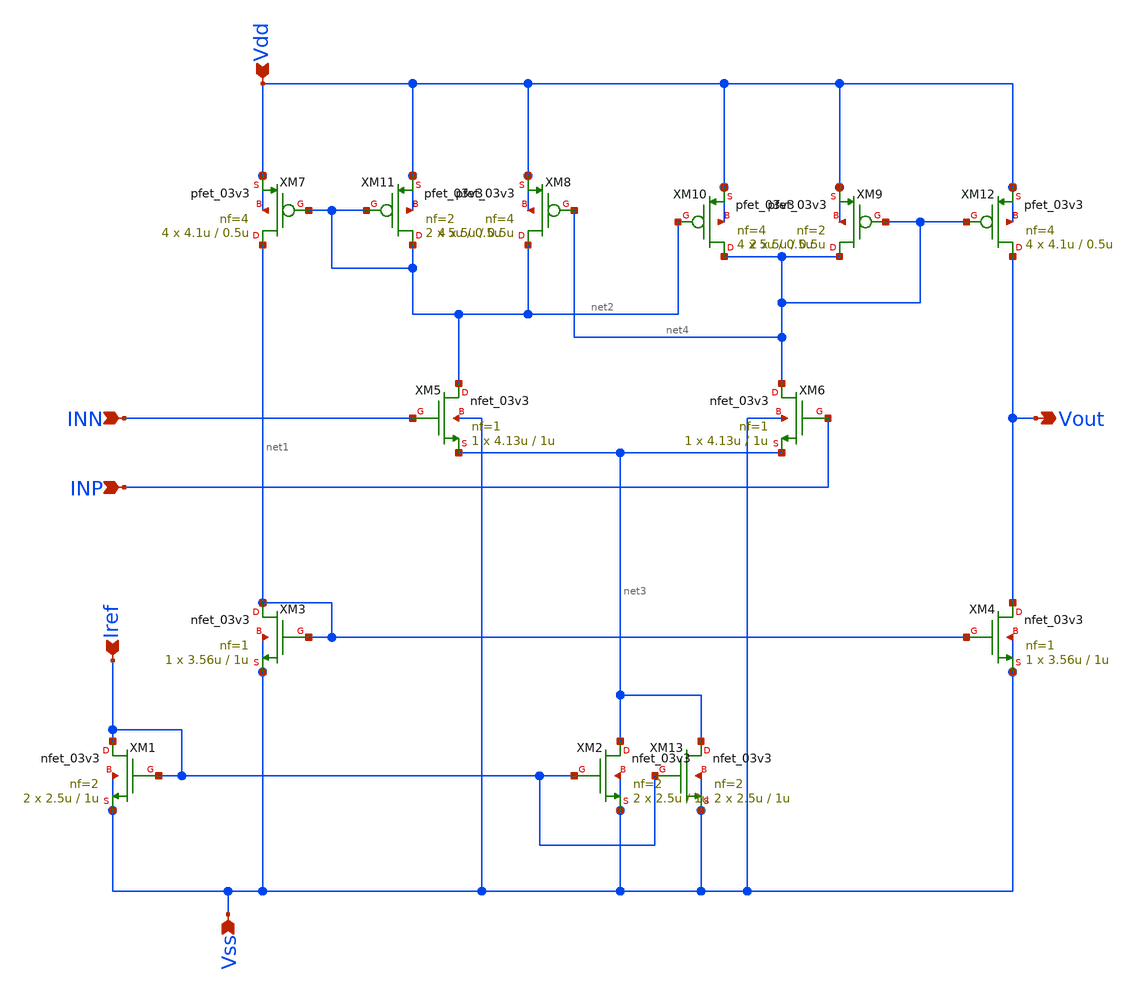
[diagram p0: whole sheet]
** sch_path: designs/libs/core_analog/Comparator/Nmos_Comparator.sch
**.subckt Nmos_Comparator Vss Vdd Iref INN INP Vout
*.ipin Vss
*.ipin Vdd
*.ipin Iref
*.ipin INN
*.ipin INP
*.opin Vout
XM3 net1 net1 Vss Vss nfet_03v3 L=1u W=3.56u nf=1 ad='int((nf+1)/2) * W/nf * 0.18u' as='int((nf+2)/2) * W/nf * 0.18u'
+ pd='2*int((nf+1)/2) * (W/nf + 0.18u)' ps='2*int((nf+2)/2) * (W/nf + 0.18u)' nrd='0.18u / W' nrs='0.18u / W'
+ sa=0 sb=0 sd=0 m=1
XM4 Vout net1 Vss Vss nfet_03v3 L=1u W=3.56u nf=1 ad='int((nf+1)/2) * W/nf * 0.18u' as='int((nf+2)/2) * W/nf * 0.18u'
+ pd='2*int((nf+1)/2) * (W/nf + 0.18u)' ps='2*int((nf+2)/2) * (W/nf + 0.18u)' nrd='0.18u / W' nrs='0.18u / W'
+ sa=0 sb=0 sd=0 m=1
XM5 net2 INN net3 Vss nfet_03v3 L=1u W=4.13u nf=1 ad='int((nf+1)/2) * W/nf * 0.18u' as='int((nf+2)/2) * W/nf * 0.18u'
+ pd='2*int((nf+1)/2) * (W/nf + 0.18u)' ps='2*int((nf+2)/2) * (W/nf + 0.18u)' nrd='0.18u / W' nrs='0.18u / W'
+ sa=0 sb=0 sd=0 m=1
XM6 net4 INP net3 Vss nfet_03v3 L=1u W=4.13u nf=1 ad='int((nf+1)/2) * W/nf * 0.18u' as='int((nf+2)/2) * W/nf * 0.18u'
+ pd='2*int((nf+1)/2) * (W/nf + 0.18u)' ps='2*int((nf+2)/2) * (W/nf + 0.18u)' nrd='0.18u / W' nrs='0.18u / W'
+ sa=0 sb=0 sd=0 m=1
XM7 net1 net2 Vdd Vdd pfet_03v3 L=0.5u W=4.1u nf=4 ad='int((nf+1)/2) * W/nf * 0.18u' as='int((nf+2)/2) * W/nf * 0.18u'
+ pd='2*int((nf+1)/2) * (W/nf + 0.18u)' ps='2*int((nf+2)/2) * (W/nf + 0.18u)' nrd='0.18u / W' nrs='0.18u / W'
+ sa=0 sb=0 sd=0 m=4
XM8 net2 net4 Vdd Vdd pfet_03v3 L=0.5u W=5u nf=4 ad='int((nf+1)/2) * W/nf * 0.18u' as='int((nf+2)/2) * W/nf * 0.18u'
+ pd='2*int((nf+1)/2) * (W/nf + 0.18u)' ps='2*int((nf+2)/2) * (W/nf + 0.18u)' nrd='0.18u / W' nrs='0.18u / W'
+ sa=0 sb=0 sd=0 m=4
XM9 net4 net4 Vdd Vdd pfet_03v3 L=0.5u W=5u nf=2 ad='int((nf+1)/2) * W/nf * 0.18u' as='int((nf+2)/2) * W/nf * 0.18u'
+ pd='2*int((nf+1)/2) * (W/nf + 0.18u)' ps='2*int((nf+2)/2) * (W/nf + 0.18u)' nrd='0.18u / W' nrs='0.18u / W'
+ sa=0 sb=0 sd=0 m=2
XM10 net4 net2 Vdd Vdd pfet_03v3 L=0.5u W=5u nf=4 ad='int((nf+1)/2) * W/nf * 0.18u' as='int((nf+2)/2) * W/nf * 0.18u'
+ pd='2*int((nf+1)/2) * (W/nf + 0.18u)' ps='2*int((nf+2)/2) * (W/nf + 0.18u)' nrd='0.18u / W' nrs='0.18u / W'
+ sa=0 sb=0 sd=0 m=4
XM11 net2 net2 Vdd Vdd pfet_03v3 L=0.5u W=5u nf=2 ad='int((nf+1)/2) * W/nf * 0.18u' as='int((nf+2)/2) * W/nf * 0.18u'
+ pd='2*int((nf+1)/2) * (W/nf + 0.18u)' ps='2*int((nf+2)/2) * (W/nf + 0.18u)' nrd='0.18u / W' nrs='0.18u / W'
+ sa=0 sb=0 sd=0 m=2
XM12 Vout net4 Vdd Vdd pfet_03v3 L=0.5u W=4.1u nf=4 ad='int((nf+1)/2) * W/nf * 0.18u' as='int((nf+2)/2) * W/nf * 0.18u'
+ pd='2*int((nf+1)/2) * (W/nf + 0.18u)' ps='2*int((nf+2)/2) * (W/nf + 0.18u)' nrd='0.18u / W' nrs='0.18u / W'
+ sa=0 sb=0 sd=0 m=4
XM1 Iref Iref Vss Vss nfet_03v3 L=1u W=2.5u nf=2 ad='int((nf+1)/2) * W/nf * 0.18u' as='int((nf+2)/2) * W/nf * 0.18u'
+ pd='2*int((nf+1)/2) * (W/nf + 0.18u)' ps='2*int((nf+2)/2) * (W/nf + 0.18u)' nrd='0.18u / W' nrs='0.18u / W'
+ sa=0 sb=0 sd=0 m=2
XM2 net3 Iref Vss Vss nfet_03v3 L=1u W=2.5u nf=2 ad='int((nf+1)/2) * W/nf * 0.18u' as='int((nf+2)/2) * W/nf * 0.18u'
+ pd='2*int((nf+1)/2) * (W/nf + 0.18u)' ps='2*int((nf+2)/2) * (W/nf + 0.18u)' nrd='0.18u / W' nrs='0.18u / W'
+ sa=0 sb=0 sd=0 m=2
XM13 net3 Iref Vss Vss nfet_03v3 L=1u W=2.5u nf=2 ad='int((nf+1)/2) * W/nf * 0.18u' as='int((nf+2)/2) * W/nf * 0.18u'
+ pd='2*int((nf+1)/2) * (W/nf + 0.18u)' ps='2*int((nf+2)/2) * (W/nf + 0.18u)' nrd='0.18u / W' nrs='0.18u / W'
+ sa=0 sb=0 sd=0 m=2
**.ends
.end
